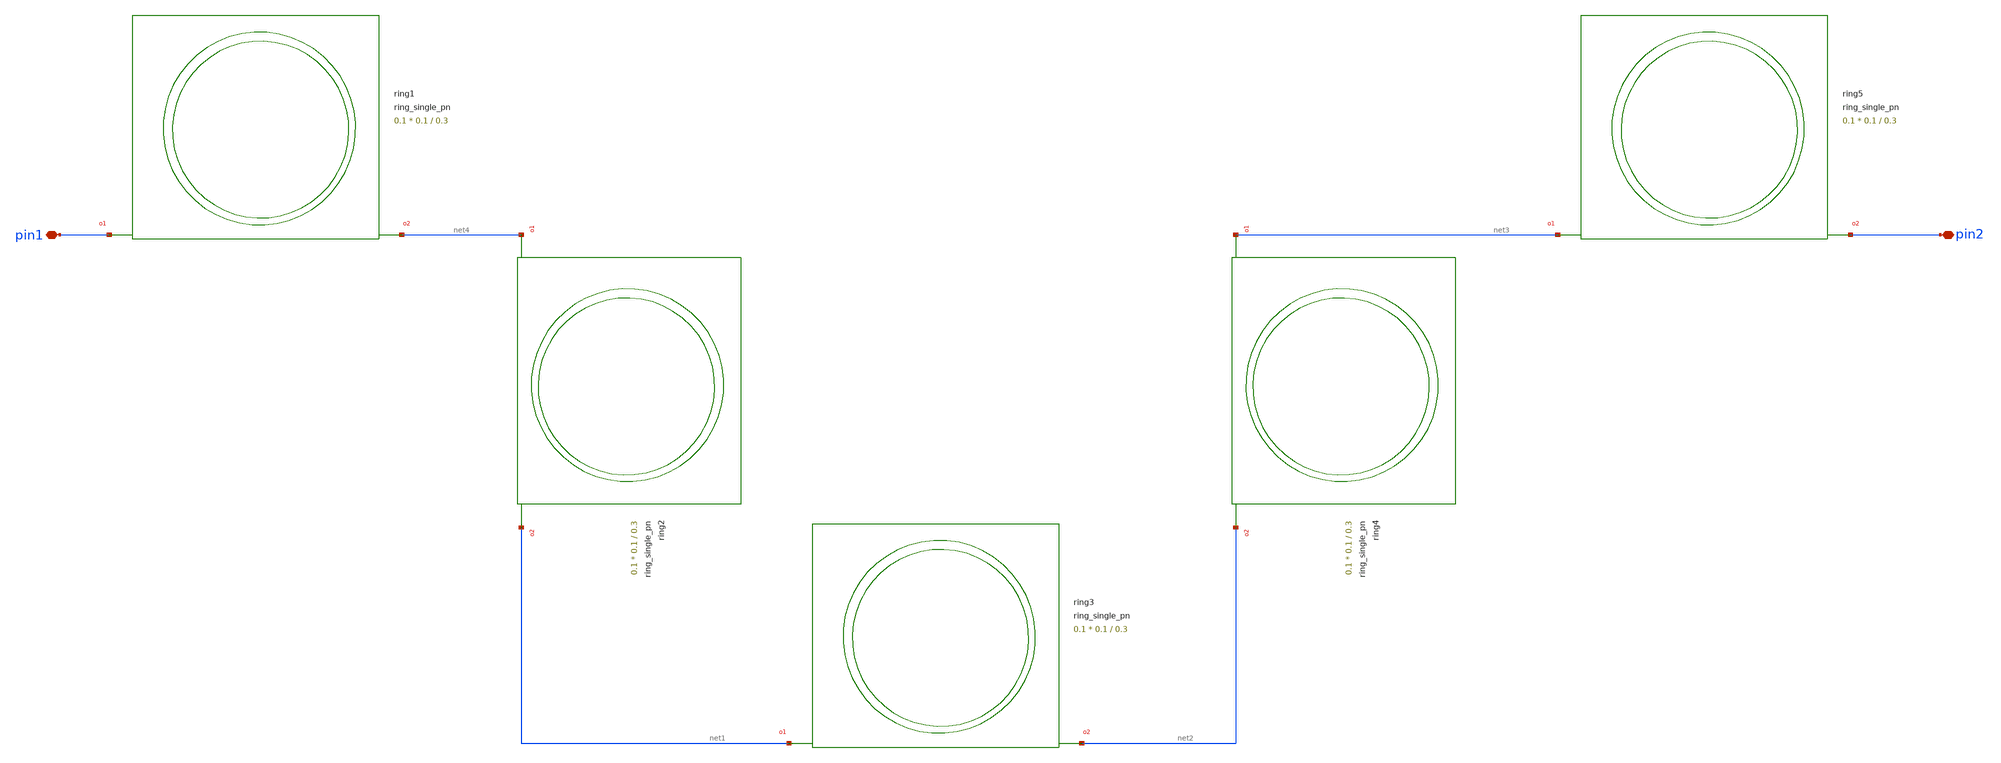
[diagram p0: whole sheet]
** sch_path: cells/xschem/tests/test_ring_single_pn.sch
* SPDX-FileCopyrightText: 2023 Mabrains Company
* Licensed under the GNU GENERAL PUBLIC License, Version 3.0 (the "License");
* you may not use this file except in compliance with the License.
* GNU GENERAL PUBLIC LICENSE
* Version 3, 29 June 2007
* This program is free software: you can redistribute it and/or modify
* it under the terms of the GNU General Public License as published
* by the Free Software Foundation, either 3 of the License, or
* (at your option) any later version.
* This program is distributed in the hope that it will be useful,
* but WITHOUT ANY WARRANTY; without even the implied warranty of
* MERCHANTABILITY or FITNESS FOR A PARTICULAR PURPOSE.  See the
* GNU General Public License for more details.
* You should have received a copy of the GNU General Public License
* along with this program.  If not, see <https://www.gnu.org/licenses/>.
* SPDX-License-Identifier: GPL-3.0
**.subckt test_ring_single_pn pin1 pin2
*.iopin pin1
*.iopin pin2
Pring1 pin1 net4 ring_single_pn gap=0.3 radius=5.0 doping_angle=250 length_x=0.1 length_y=0.1
Pring2 net4 net1 ring_single_pn gap=0.3 radius=5.0 doping_angle=250 length_x=0.1 length_y=0.1
Pring3 net1 net2 ring_single_pn gap=0.3 radius=5.0 doping_angle=250 length_x=0.1 length_y=0.1
Pring4 net3 net2 ring_single_pn gap=0.3 radius=5.0 doping_angle=250 length_x=0.1 length_y=0.1
Pring5 net3 pin2 ring_single_pn gap=0.3 radius=5.0 doping_angle=250 length_x=0.1 length_y=0.1
**.ends
.end
